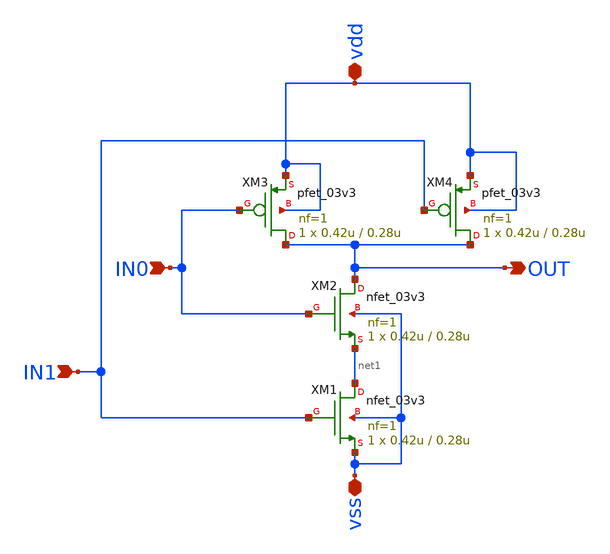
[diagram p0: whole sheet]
** sch_path: nand2.sch
**.subckt nand2 IN0 IN1 OUT vdd vss
*.ipin IN0
*.ipin IN1
*.opin OUT
*.iopin vdd
*.iopin vss
XM1 net1 IN1 vss vss nfet_03v3 L=0.28u W=0.42u nf=1 ad='int((nf+1)/2) * W/nf * 0.18u' as='int((nf+2)/2) * W/nf * 0.18u'
+ pd='2*int((nf+1)/2) * (W/nf + 0.18u)' ps='2*int((nf+2)/2) * (W/nf + 0.18u)' nrd='0.18u / W' nrs='0.18u / W'
+ sa=0 sb=0 sd=0 m=1
XM3 OUT IN0 vdd vdd pfet_03v3 L=0.28u W=0.42u nf=1 ad='int((nf+1)/2) * W/nf * 0.18u' as='int((nf+2)/2) * W/nf * 0.18u'
+ pd='2*int((nf+1)/2) * (W/nf + 0.18u)' ps='2*int((nf+2)/2) * (W/nf + 0.18u)' nrd='0.18u / W' nrs='0.18u / W'
+ sa=0 sb=0 sd=0 m=1
XM4 OUT IN1 vdd vdd pfet_03v3 L=0.28u W=0.42u nf=1 ad='int((nf+1)/2) * W/nf * 0.18u' as='int((nf+2)/2) * W/nf * 0.18u'
+ pd='2*int((nf+1)/2) * (W/nf + 0.18u)' ps='2*int((nf+2)/2) * (W/nf + 0.18u)' nrd='0.18u / W' nrs='0.18u / W'
+ sa=0 sb=0 sd=0 m=1
XM2 OUT IN0 net1 vss nfet_03v3 L=0.28u W=0.42u nf=1 ad='int((nf+1)/2) * W/nf * 0.18u' as='int((nf+2)/2) * W/nf * 0.18u'
+ pd='2*int((nf+1)/2) * (W/nf + 0.18u)' ps='2*int((nf+2)/2) * (W/nf + 0.18u)' nrd='0.18u / W' nrs='0.18u / W'
+ sa=0 sb=0 sd=0 m=1
**.ends
.end
